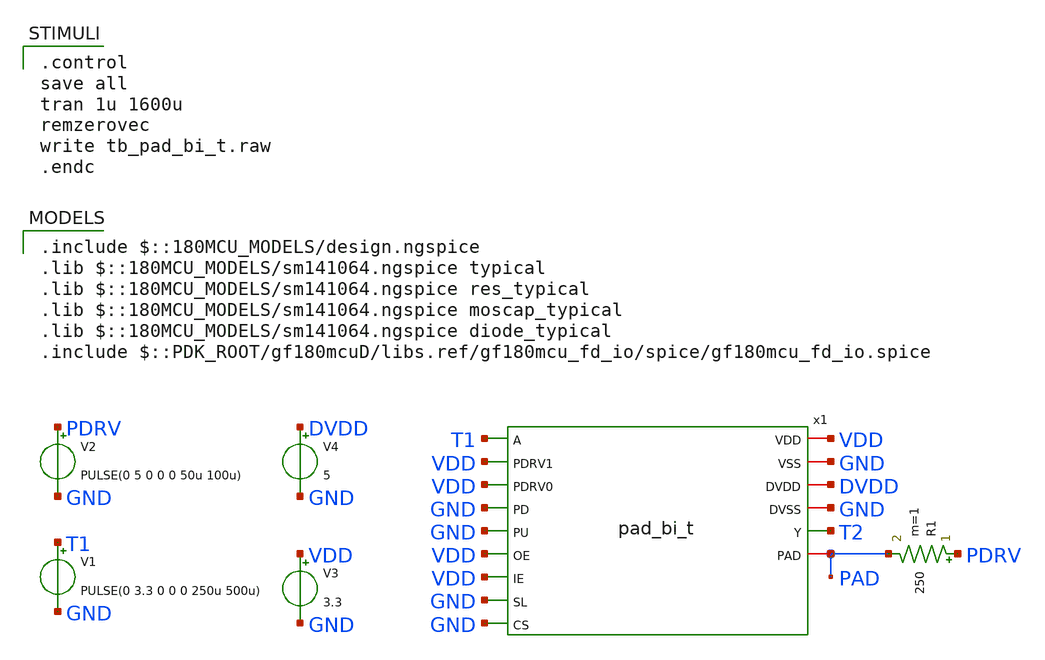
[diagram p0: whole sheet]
** sch_path: pads/tb_pad_bi_t.sch
**.subckt tb_pad_bi_t
x1 T1 VDD VDD GND GND VDD GND VDD VDD DVDD GND GND T2 PAD GND pad_bi_t
V3 VDD GND 3.3
V1 T1 GND PULSE(0 3.3 0 0 0 250u 500u)
R1 PDRV PAD 250 m=1
V2 PDRV GND PULSE(0 5 0 0 0 50u 100u)
V4 DVDD GND 5
**** begin user architecture code
 .include $::180MCU_MODELS/design.ngspice
.lib $::180MCU_MODELS/sm141064.ngspice typical
.lib $::180MCU_MODELS/sm141064.ngspice res_typical
.lib $::180MCU_MODELS/sm141064.ngspice moscap_typical
.lib $::180MCU_MODELS/sm141064.ngspice diode_typical
.include $::PDK_ROOT/gf180mcuD/libs.ref/gf180mcu_fd_io/spice/gf180mcu_fd_io.spice


.control
save all
tran 1u 1600u
remzerovec
write tb_pad_bi_t.raw
.endc

**** end user architecture code
**.ends

* expanding   symbol:  pad_bi_t.sym # of pins=15
** sym_path: pads/pad_bi_t.sym
.subckt pad_bi_t A CS DVDD DVSS IE OE PAD PD PDRV0 PDRV1 PU SL VDD VSS Y
x1 A CS DVDD DVSS IE OE PAD PD PDRV0 PDRV1 PU SL VDD VSS Y gf180mcu_fd_io__bi_t
.ends
.end
